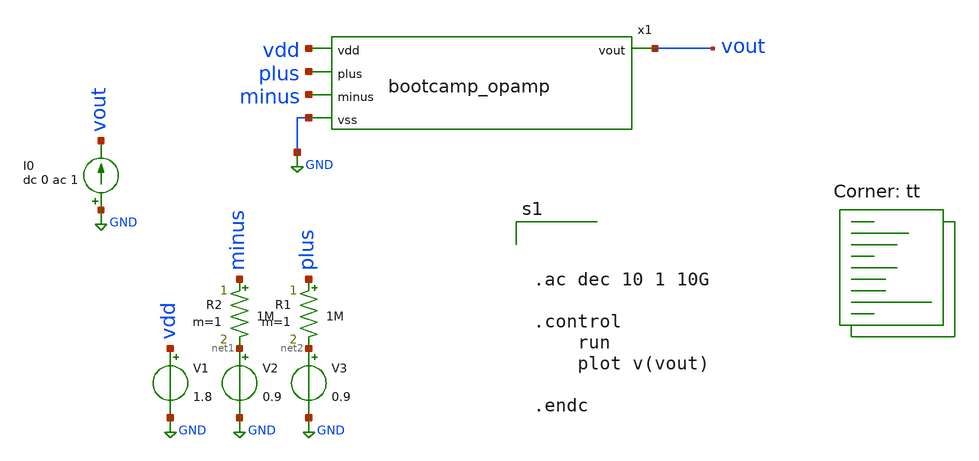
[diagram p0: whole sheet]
** sch_path: analog/schematics/bootcamp_opamp_tb_impedance.sch
**.subckt bootcamp_opamp_tb_impedance
V1 vdd GND 1.8
V2 net1 GND 0.9
V3 net2 GND 0.9
I0 GND vout dc 0 ac 1
R2 minus net1 1M m=1
R1 plus net2 1M m=1
x1 vdd vout plus minus GND bootcamp_opamp
**** begin user architecture code



.ac dec 10 1 10G

.control
	run
	plot v(vout)

.endc




.lib $::SKYWATER_MODELS/sky130.lib.spice tt
**** end user architecture code
**.ends

* expanding   symbol:  bootcamp_opamp.sym # of pins=5
** sym_path: analog/schematics/bootcamp_opamp.sym
** sch_path: analog/schematics/bootcamp_opamp.sch
.subckt bootcamp_opamp vdd vout plus minus vss
*.ipin vdd
*.ipin minus
*.ipin plus
*.ipin vss
*.opin vout
XM1 net2 minus net1 net1 sky130_fd_pr__nfet_01v8 L=1 W=10 nf=1 ad='int((nf+1)/2) * W/nf * 0.29' as='int((nf+2)/2) * W/nf * 0.29'
+ pd='2*int((nf+1)/2) * (W/nf + 0.29)' ps='2*int((nf+2)/2) * (W/nf + 0.29)' nrd='0.29 / W' nrs='0.29 / W'
+ sa=0 sb=0 sd=0 mult=1 m=1
I0 vdd net4 50u
XM4 net3 plus net1 net1 sky130_fd_pr__nfet_01v8 L=1 W=10 nf=1 ad='int((nf+1)/2) * W/nf * 0.29' as='int((nf+2)/2) * W/nf * 0.29'
+ pd='2*int((nf+1)/2) * (W/nf + 0.29)' ps='2*int((nf+2)/2) * (W/nf + 0.29)' nrd='0.29 / W' nrs='0.29 / W'
+ sa=0 sb=0 sd=0 mult=1 m=1
XM5 net2 net2 vdd vdd sky130_fd_pr__pfet_01v8 L=1 W=10 nf=1 ad='int((nf+1)/2) * W/nf * 0.29' as='int((nf+2)/2) * W/nf * 0.29'
+ pd='2*int((nf+1)/2) * (W/nf + 0.29)' ps='2*int((nf+2)/2) * (W/nf + 0.29)' nrd='0.29 / W' nrs='0.29 / W'
+ sa=0 sb=0 sd=0 mult=1 m=1
XM6 net3 net2 vdd vdd sky130_fd_pr__pfet_01v8 L=1 W=10 nf=1 ad='int((nf+1)/2) * W/nf * 0.29' as='int((nf+2)/2) * W/nf * 0.29'
+ pd='2*int((nf+1)/2) * (W/nf + 0.29)' ps='2*int((nf+2)/2) * (W/nf + 0.29)' nrd='0.29 / W' nrs='0.29 / W'
+ sa=0 sb=0 sd=0 mult=1 m=1
XM2 net4 net4 vss vss sky130_fd_pr__nfet_01v8 L=0.15 W=1 nf=1 ad='int((nf+1)/2) * W/nf * 0.29' as='int((nf+2)/2) * W/nf * 0.29'
+ pd='2*int((nf+1)/2) * (W/nf + 0.29)' ps='2*int((nf+2)/2) * (W/nf + 0.29)' nrd='0.29 / W' nrs='0.29 / W'
+ sa=0 sb=0 sd=0 mult=1 m=1
XM7 net1 net4 vss vss sky130_fd_pr__nfet_01v8 L=1 W=5 nf=1 ad='int((nf+1)/2) * W/nf * 0.29' as='int((nf+2)/2) * W/nf * 0.29'
+ pd='2*int((nf+1)/2) * (W/nf + 0.29)' ps='2*int((nf+2)/2) * (W/nf + 0.29)' nrd='0.29 / W' nrs='0.29 / W'
+ sa=0 sb=0 sd=0 mult=1 m=1
XM3 vout net4 vss vss sky130_fd_pr__nfet_01v8 L=1 W=25 nf=1 ad='int((nf+1)/2) * W/nf * 0.29' as='int((nf+2)/2) * W/nf * 0.29'
+ pd='2*int((nf+1)/2) * (W/nf + 0.29)' ps='2*int((nf+2)/2) * (W/nf + 0.29)' nrd='0.29 / W' nrs='0.29 / W'
+ sa=0 sb=0 sd=0 mult=1 m=1
XM8 vout net3 vdd vdd sky130_fd_pr__pfet_01v8 L=1 W=100 nf=1 ad='int((nf+1)/2) * W/nf * 0.29' as='int((nf+2)/2) * W/nf * 0.29'
+ pd='2*int((nf+1)/2) * (W/nf + 0.29)' ps='2*int((nf+2)/2) * (W/nf + 0.29)' nrd='0.29 / W' nrs='0.29 / W'
+ sa=0 sb=0 sd=0 mult=1 m=1
.ends

.GLOBAL GND
.end
